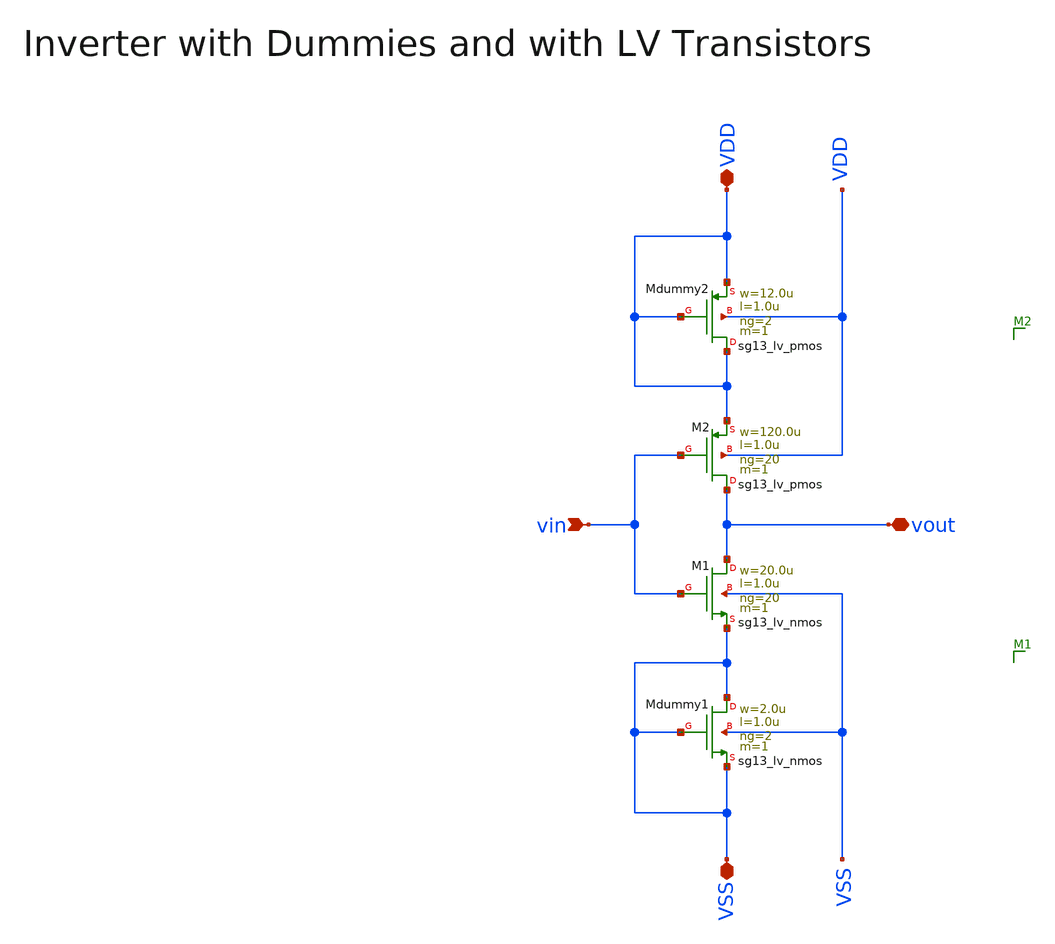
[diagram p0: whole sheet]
** sch_path: ihp130/macros/iqmod/schematic/xschem/iqmod_mfb_lpf_ota_core_inv_NF20.sch
**.subckt iqmod_mfb_lpf_ota_core_inv_NF20 vin VDD VSS vout
*.ipin vin
*.iopin VDD
*.iopin VSS
*.iopin vout
XMdummy1 VSS VSS VSS VSS sg13_lv_nmos w=2.0u l=1.0u ng=2 m=1 mm_ok=1
XMdummy2 VDD VDD VDD VDD sg13_lv_pmos w=12.0u l=1.0u ng=2 m=1 mm_ok=1
XM1 vout vin VSS VSS sg13_lv_nmos w=20.0u l=1.0u ng=20 m=1 mm_ok=1
XM2 vout vin VDD VDD sg13_lv_pmos w=120.0u l=1.0u ng=20 m=1 mm_ok=1
**.ends
.end
